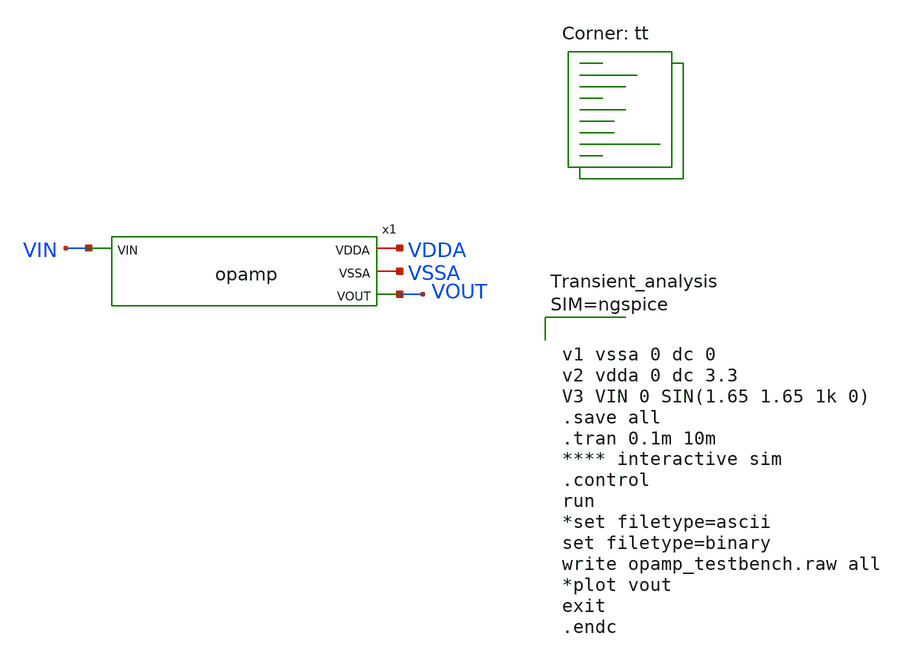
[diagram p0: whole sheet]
** sch_path: Rail_Rail_opamp_3v3/Schematic/opamp_testbench.sch
**.subckt opamp_testbench
x1 VDDA VSSA VIN VOUT opamp
**** begin user architecture code
.lib $::SKYWATER_MODELS/sky130.lib.spice tt



v1 vssa 0 dc 0
v2 vdda 0 dc 3.3
V3 VIN 0 SIN(1.65 1.65 1k 0)
.save all
.tran 0.1m 10m
**** interactive sim
.control
run
*set filetype=ascii
set filetype=binary
write opamp_testbench.raw all
*plot vout
exit
.endc



**** end user architecture code
**.ends
.end
